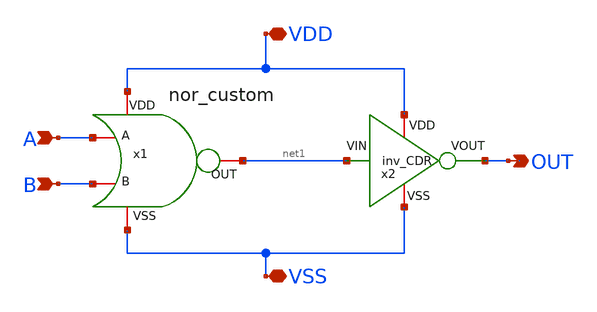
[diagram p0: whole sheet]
** sch_path: CDR4176-main/schematic/xschem/or_custom/or_custom.sch
**.subckt or_custom VDD VSS OUT A B
*.iopin VDD
*.iopin VSS
*.opin OUT
*.ipin A
*.ipin B
x1 VDD A net1 B VSS nor_custom
x2 VDD OUT net1 VSS inv_CDR
**.ends
.end
